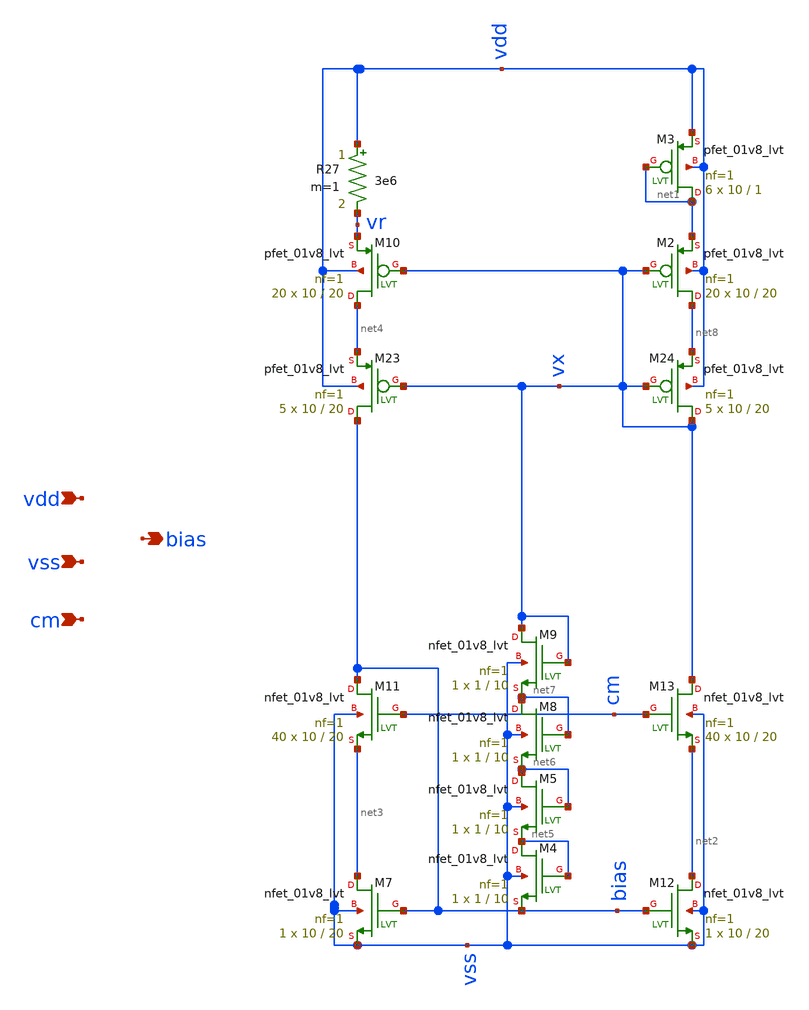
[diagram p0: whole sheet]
** sch_path: Bias_Core.sch
**.subckt Bias_Core vdd vss bias cm
*.ipin vdd
*.ipin vss
*.opin bias
*.ipin cm
XM7 net3 bias vss vss sky130_fd_pr__nfet_01v8_lvt L=20 W=10 nf=1 ad='int((nf+1)/2) * W/nf * 0.29' as='int((nf+2)/2) * W/nf * 0.29'
+ pd='2*int((nf+1)/2) * (W/nf + 0.29)' ps='2*int((nf+2)/2) * (W/nf + 0.29)' nrd='0.29 / W' nrs='0.29 / W'
+ sa=0 sb=0 sd=0 mult=1 m=1
XM10 net4 vx vr vdd sky130_fd_pr__pfet_01v8_lvt L=20 W=10 nf=1 ad='int((nf+1)/2) * W/nf * 0.29' as='int((nf+2)/2) * W/nf * 0.29'
+ pd='2*int((nf+1)/2) * (W/nf + 0.29)' ps='2*int((nf+2)/2) * (W/nf + 0.29)' nrd='0.29 / W' nrs='0.29 / W'
+ sa=0 sb=0 sd=0 mult=20 m=20
XM11 bias cm net3 vss sky130_fd_pr__nfet_01v8_lvt L=20 W=10 nf=1 ad='int((nf+1)/2) * W/nf * 0.29' as='int((nf+2)/2) * W/nf * 0.29'
+ pd='2*int((nf+1)/2) * (W/nf + 0.29)' ps='2*int((nf+2)/2) * (W/nf + 0.29)' nrd='0.29 / W' nrs='0.29 / W'
+ sa=0 sb=0 sd=0 mult=40 m=40
XM12 net2 bias vss vss sky130_fd_pr__nfet_01v8_lvt L=20 W=10 nf=1 ad='int((nf+1)/2) * W/nf * 0.29' as='int((nf+2)/2) * W/nf * 0.29'
+ pd='2*int((nf+1)/2) * (W/nf + 0.29)' ps='2*int((nf+2)/2) * (W/nf + 0.29)' nrd='0.29 / W' nrs='0.29 / W'
+ sa=0 sb=0 sd=0 mult=1 m=1
XM13 vx cm net2 vss sky130_fd_pr__nfet_01v8_lvt L=20 W=10 nf=1 ad='int((nf+1)/2) * W/nf * 0.29' as='int((nf+2)/2) * W/nf * 0.29'
+ pd='2*int((nf+1)/2) * (W/nf + 0.29)' ps='2*int((nf+2)/2) * (W/nf + 0.29)' nrd='0.29 / W' nrs='0.29 / W'
+ sa=0 sb=0 sd=0 mult=40 m=40
XM2 net8 vx net1 vdd sky130_fd_pr__pfet_01v8_lvt L=20 W=10 nf=1 ad='int((nf+1)/2) * W/nf * 0.29' as='int((nf+2)/2) * W/nf * 0.29'
+ pd='2*int((nf+1)/2) * (W/nf + 0.29)' ps='2*int((nf+2)/2) * (W/nf + 0.29)' nrd='0.29 / W' nrs='0.29 / W'
+ sa=0 sb=0 sd=0 mult=20 m=20
XM3 net1 net1 vdd vdd sky130_fd_pr__pfet_01v8_lvt L=1 W=10 nf=1 ad='int((nf+1)/2) * W/nf * 0.29' as='int((nf+2)/2) * W/nf * 0.29'
+ pd='2*int((nf+1)/2) * (W/nf + 0.29)' ps='2*int((nf+2)/2) * (W/nf + 0.29)' nrd='0.29 / W' nrs='0.29 / W'
+ sa=0 sb=0 sd=0 mult=6 m=6
XM4 net5 net5 bias vss sky130_fd_pr__nfet_01v8_lvt L=10 W=1 nf=1 ad='int((nf+1)/2) * W/nf * 0.29' as='int((nf+2)/2) * W/nf * 0.29'
+ pd='2*int((nf+1)/2) * (W/nf + 0.29)' ps='2*int((nf+2)/2) * (W/nf + 0.29)' nrd='0.29 / W' nrs='0.29 / W'
+ sa=0 sb=0 sd=0 mult=1 m=1
XM5 net6 net6 net5 vss sky130_fd_pr__nfet_01v8_lvt L=10 W=1 nf=1 ad='int((nf+1)/2) * W/nf * 0.29' as='int((nf+2)/2) * W/nf * 0.29'
+ pd='2*int((nf+1)/2) * (W/nf + 0.29)' ps='2*int((nf+2)/2) * (W/nf + 0.29)' nrd='0.29 / W' nrs='0.29 / W'
+ sa=0 sb=0 sd=0 mult=1 m=1
XM8 net7 net7 net6 vss sky130_fd_pr__nfet_01v8_lvt L=10 W=1 nf=1 ad='int((nf+1)/2) * W/nf * 0.29' as='int((nf+2)/2) * W/nf * 0.29'
+ pd='2*int((nf+1)/2) * (W/nf + 0.29)' ps='2*int((nf+2)/2) * (W/nf + 0.29)' nrd='0.29 / W' nrs='0.29 / W'
+ sa=0 sb=0 sd=0 mult=1 m=1
XM9 vx vx net7 vss sky130_fd_pr__nfet_01v8_lvt L=10 W=1 nf=1 ad='int((nf+1)/2) * W/nf * 0.29' as='int((nf+2)/2) * W/nf * 0.29'
+ pd='2*int((nf+1)/2) * (W/nf + 0.29)' ps='2*int((nf+2)/2) * (W/nf + 0.29)' nrd='0.29 / W' nrs='0.29 / W'
+ sa=0 sb=0 sd=0 mult=1 m=1
XM23 bias vx net4 vdd sky130_fd_pr__pfet_01v8_lvt L=20 W=10 nf=1 ad='int((nf+1)/2) * W/nf * 0.29' as='int((nf+2)/2) * W/nf * 0.29'
+ pd='2*int((nf+1)/2) * (W/nf + 0.29)' ps='2*int((nf+2)/2) * (W/nf + 0.29)' nrd='0.29 / W' nrs='0.29 / W'
+ sa=0 sb=0 sd=0 mult=5 m=5
XM24 vx vx net8 vdd sky130_fd_pr__pfet_01v8_lvt L=20 W=10 nf=1 ad='int((nf+1)/2) * W/nf * 0.29' as='int((nf+2)/2) * W/nf * 0.29'
+ pd='2*int((nf+1)/2) * (W/nf + 0.29)' ps='2*int((nf+2)/2) * (W/nf + 0.29)' nrd='0.29 / W' nrs='0.29 / W'
+ sa=0 sb=0 sd=0 mult=5 m=5
R27 vdd vr 3e6 m=1
**.ends
.end
